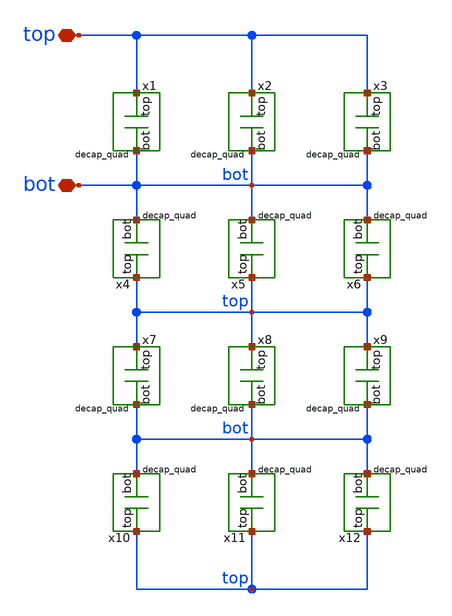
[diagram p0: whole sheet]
** sch_path: v2_feature_extr_withf/decap_unit.sch
**.subckt decap_unit top bot
*.iopin top
*.iopin bot
x1 top bot decap_quad
x2 top bot decap_quad
x3 top bot decap_quad
x4 top bot decap_quad
x5 top bot decap_quad
x6 top bot decap_quad
x7 top bot decap_quad
x8 top bot decap_quad
x9 top bot decap_quad
x10 top bot decap_quad
x11 top bot decap_quad
x12 top bot decap_quad
**.ends
.end
